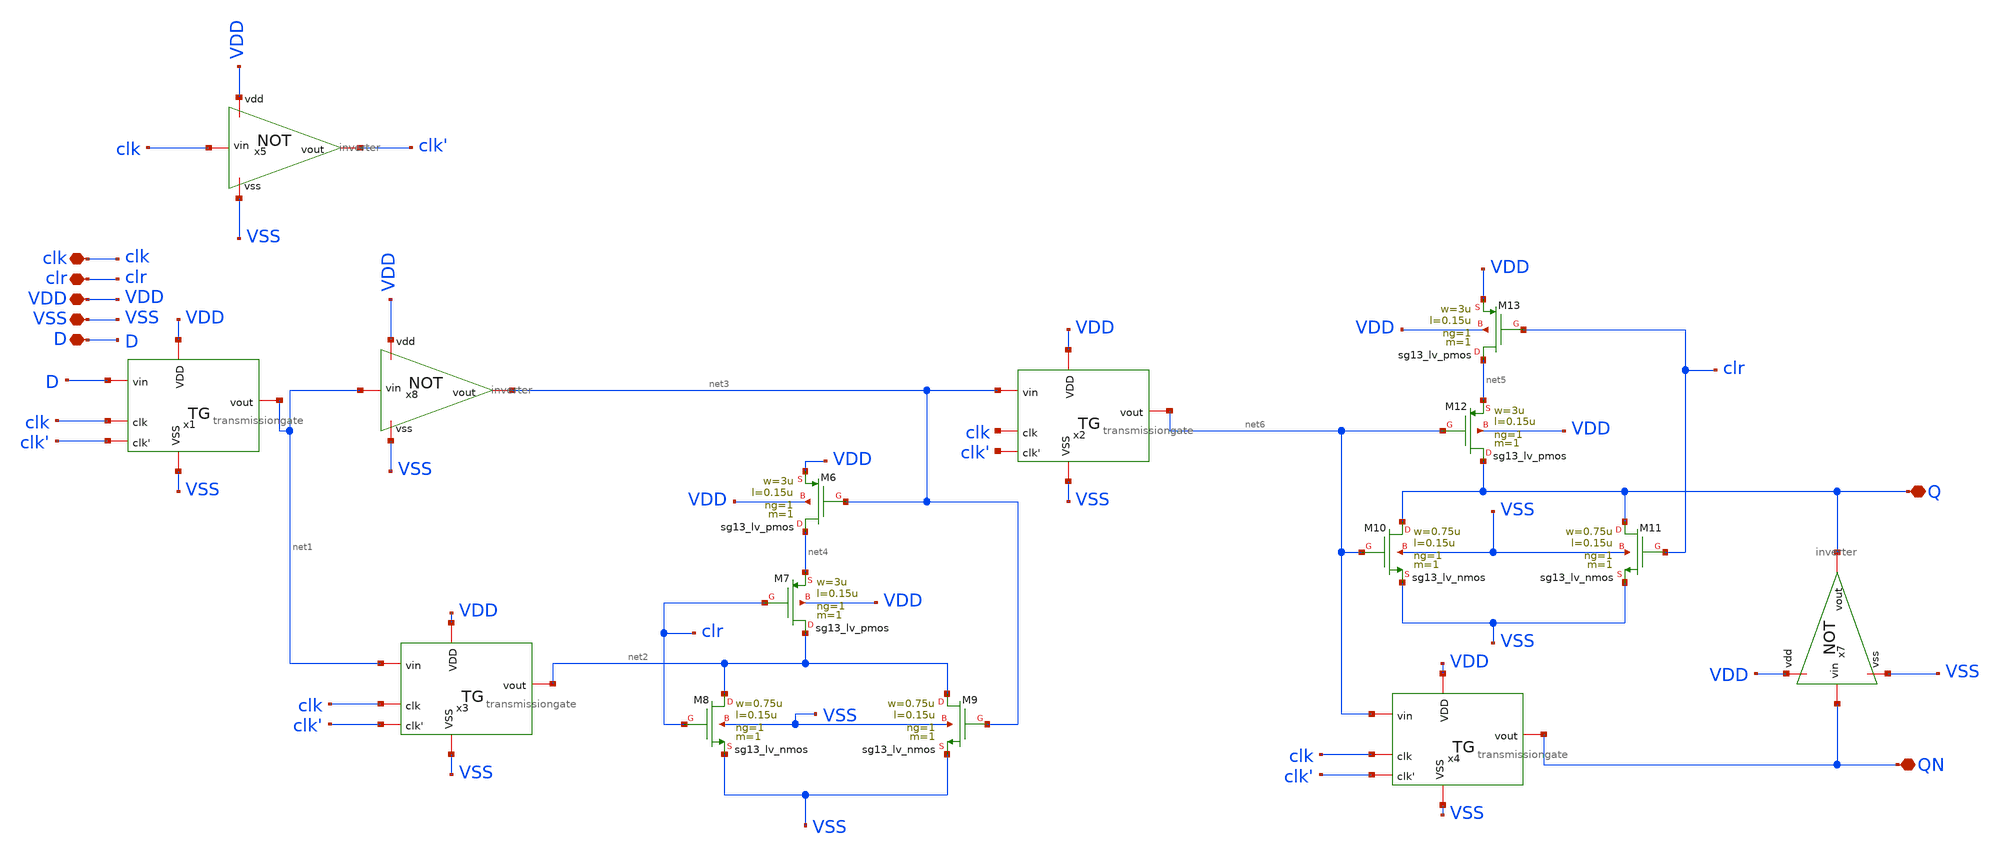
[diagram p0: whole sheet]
** sch_path: design/blocks/flipflop-D/DFFC.sch
**.subckt DFFC clk clr VDD Q QN VSS D
*.iopin clk
*.iopin clr
*.iopin VDD
*.iopin Q
*.iopin QN
*.iopin VSS
*.iopin D
XM8 net2 clr VSS VSS sg13_lv_nmos w=0.75u l=0.15u ng=1 m=1 mm_ok=1
XM9 net2 net3 VSS VSS sg13_lv_nmos w=0.75u l=0.15u ng=1 m=1 mm_ok=1
XM7 net2 clr net4 VDD sg13_lv_pmos w=3u l=0.15u ng=1 m=1 mm_ok=1
XM6 net4 net3 VDD VDD sg13_lv_pmos w=3u l=0.15u ng=1 m=1 mm_ok=1
XM10 Q net6 VSS VSS sg13_lv_nmos w=0.75u l=0.15u ng=1 m=1 mm_ok=1
XM11 Q clr VSS VSS sg13_lv_nmos w=0.75u l=0.15u ng=1 m=1 mm_ok=1
XM12 Q net6 net5 VDD sg13_lv_pmos w=3u l=0.15u ng=1 m=1 mm_ok=1
XM13 net5 clr VDD VDD sg13_lv_pmos w=3u l=0.15u ng=1 m=1 mm_ok=1
x8 VDD net3 net1 VSS inverter
x5 VDD clk' clk VSS inverter
x7 VDD Q QN VSS inverter
x1 clk VSS D net1 VDD clk' transmissiongate
x2 clk VSS net3 net6 VDD clk' transmissiongate
x3 clk VSS net1 net2 VDD clk' transmissiongate
x4 clk VSS net6 QN VDD clk' transmissiongate
**.ends

* expanding   symbol:  blocks/inverter/inverter.sym # of pins=4
** sym_path: design/blocks/inverter/inverter.sym
** sch_path: design/blocks/inverter/inverter.sch
.subckt inverter vdd vout vin vss
*.iopin vdd
*.iopin vout
*.iopin vss
*.iopin vin
XM1 vout vin vss vss sg13_lv_nmos w=0.75u l=0.15u ng=1 m=1 mm_ok=1
XM2 vout vin vdd vdd sg13_lv_pmos w=1.5u l=0.15u ng=1 m=1 mm_ok=1
.ends


* expanding   symbol:  blocks/transmissiongate/transmissiongate.sym # of pins=6
** sym_path: design/blocks/transmissiongate/transmissiongate.sym
** sch_path: design/blocks/transmissiongate/transmissiongate.sch
.subckt transmissiongate clk VSS vin vout VDD clk'
*.iopin vout
*.iopin vin
*.iopin clk
*.iopin clk'
*.iopin VSS
*.iopin VDD
XM1 vout clk' vin VDD sg13_lv_pmos w=1.5u l=0.15u ng=1 m=1 mm_ok=1
XM0 vin clk vout VSS sg13_lv_nmos w=0.75u l=0.15u ng=1 m=1 mm_ok=1
.ends

.end
